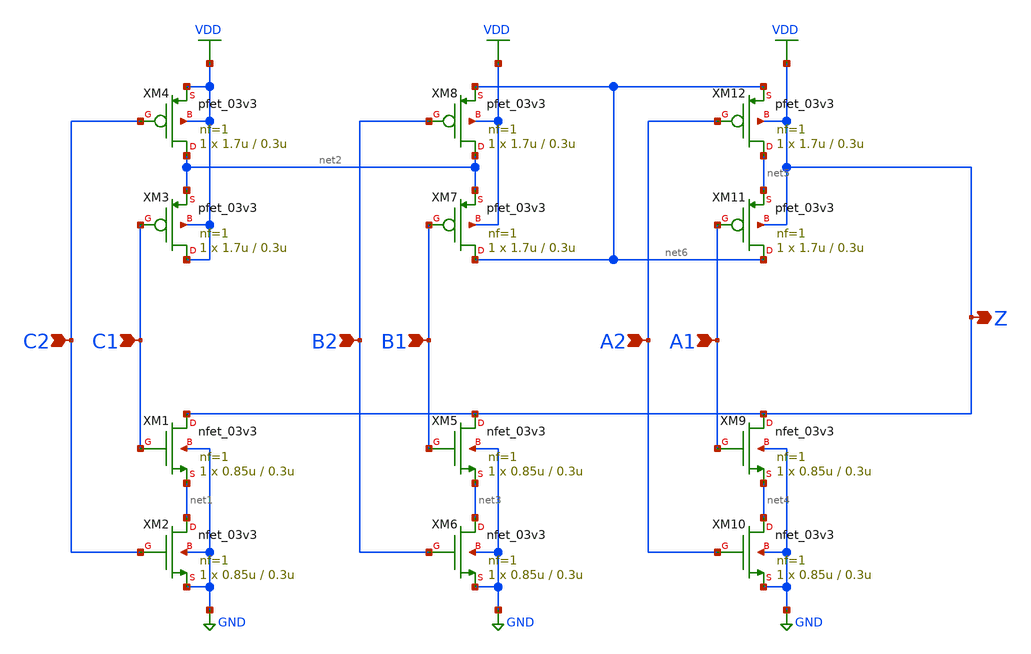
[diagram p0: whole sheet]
** sch_path: aoi222/aoi222_1.sch
**.subckt aoi222_1 C1 C2 B1 B2 A1 A2 Z
*.ipin C1
*.ipin C2
*.ipin B1
*.ipin B2
*.ipin A1
*.ipin A2
*.opin Z
XM1 VDD C1 net1 GND nfet_03v3 L=0.3u W=0.85u nf=1 ad='int((nf+1)/2) * W/nf * 0.18u' as='int((nf+2)/2) * W/nf * 0.18u'
+ pd='2*int((nf+1)/2) * (W/nf + 0.18u)' ps='2*int((nf+2)/2) * (W/nf + 0.18u)' nrd='0.18u / W' nrs='0.18u / W'
+ sa=0 sb=0 sd=0 m=1
XM2 net1 C2 GND GND nfet_03v3 L=0.3u W=0.85u nf=1 ad='int((nf+1)/2) * W/nf * 0.18u' as='int((nf+2)/2) * W/nf * 0.18u'
+ pd='2*int((nf+1)/2) * (W/nf + 0.18u)' ps='2*int((nf+2)/2) * (W/nf + 0.18u)' nrd='0.18u / W' nrs='0.18u / W'
+ sa=0 sb=0 sd=0 m=1
XM3 VDD C1 net2 VDD pfet_03v3 L=0.3u W=1.7u nf=1 ad='int((nf+1)/2) * W/nf * 0.18u' as='int((nf+2)/2) * W/nf * 0.18u'
+ pd='2*int((nf+1)/2) * (W/nf + 0.18u)' ps='2*int((nf+2)/2) * (W/nf + 0.18u)' nrd='0.18u / W' nrs='0.18u / W'
+ sa=0 sb=0 sd=0 m=1
XM4 net2 C2 VDD VDD pfet_03v3 L=0.3u W=1.7u nf=1 ad='int((nf+1)/2) * W/nf * 0.18u' as='int((nf+2)/2) * W/nf * 0.18u'
+ pd='2*int((nf+1)/2) * (W/nf + 0.18u)' ps='2*int((nf+2)/2) * (W/nf + 0.18u)' nrd='0.18u / W' nrs='0.18u / W'
+ sa=0 sb=0 sd=0 m=1
XM5 VDD B1 net3 GND nfet_03v3 L=0.3u W=0.85u nf=1 ad='int((nf+1)/2) * W/nf * 0.18u' as='int((nf+2)/2) * W/nf * 0.18u'
+ pd='2*int((nf+1)/2) * (W/nf + 0.18u)' ps='2*int((nf+2)/2) * (W/nf + 0.18u)' nrd='0.18u / W' nrs='0.18u / W'
+ sa=0 sb=0 sd=0 m=1
XM6 net3 B2 GND GND nfet_03v3 L=0.3u W=0.85u nf=1 ad='int((nf+1)/2) * W/nf * 0.18u' as='int((nf+2)/2) * W/nf * 0.18u'
+ pd='2*int((nf+1)/2) * (W/nf + 0.18u)' ps='2*int((nf+2)/2) * (W/nf + 0.18u)' nrd='0.18u / W' nrs='0.18u / W'
+ sa=0 sb=0 sd=0 m=1
XM7 net6 B1 net2 VDD pfet_03v3 L=0.3u W=1.7u nf=1 ad='int((nf+1)/2) * W/nf * 0.18u' as='int((nf+2)/2) * W/nf * 0.18u'
+ pd='2*int((nf+1)/2) * (W/nf + 0.18u)' ps='2*int((nf+2)/2) * (W/nf + 0.18u)' nrd='0.18u / W' nrs='0.18u / W'
+ sa=0 sb=0 sd=0 m=1
XM8 net2 B2 net6 VDD pfet_03v3 L=0.3u W=1.7u nf=1 ad='int((nf+1)/2) * W/nf * 0.18u' as='int((nf+2)/2) * W/nf * 0.18u'
+ pd='2*int((nf+1)/2) * (W/nf + 0.18u)' ps='2*int((nf+2)/2) * (W/nf + 0.18u)' nrd='0.18u / W' nrs='0.18u / W'
+ sa=0 sb=0 sd=0 m=1
XM9 VDD A1 net4 GND nfet_03v3 L=0.3u W=0.85u nf=1 ad='int((nf+1)/2) * W/nf * 0.18u' as='int((nf+2)/2) * W/nf * 0.18u'
+ pd='2*int((nf+1)/2) * (W/nf + 0.18u)' ps='2*int((nf+2)/2) * (W/nf + 0.18u)' nrd='0.18u / W' nrs='0.18u / W'
+ sa=0 sb=0 sd=0 m=1
XM10 net4 A2 GND GND nfet_03v3 L=0.3u W=0.85u nf=1 ad='int((nf+1)/2) * W/nf * 0.18u' as='int((nf+2)/2) * W/nf * 0.18u'
+ pd='2*int((nf+1)/2) * (W/nf + 0.18u)' ps='2*int((nf+2)/2) * (W/nf + 0.18u)' nrd='0.18u / W' nrs='0.18u / W'
+ sa=0 sb=0 sd=0 m=1
XM11 net6 A1 net5 VDD pfet_03v3 L=0.3u W=1.7u nf=1 ad='int((nf+1)/2) * W/nf * 0.18u' as='int((nf+2)/2) * W/nf * 0.18u'
+ pd='2*int((nf+1)/2) * (W/nf + 0.18u)' ps='2*int((nf+2)/2) * (W/nf + 0.18u)' nrd='0.18u / W' nrs='0.18u / W'
+ sa=0 sb=0 sd=0 m=1
XM12 net5 A2 net6 VDD pfet_03v3 L=0.3u W=1.7u nf=1 ad='int((nf+1)/2) * W/nf * 0.18u' as='int((nf+2)/2) * W/nf * 0.18u'
+ pd='2*int((nf+1)/2) * (W/nf + 0.18u)' ps='2*int((nf+2)/2) * (W/nf + 0.18u)' nrd='0.18u / W' nrs='0.18u / W'
+ sa=0 sb=0 sd=0 m=1
**.ends
.GLOBAL GND
.GLOBAL VDD
.end
